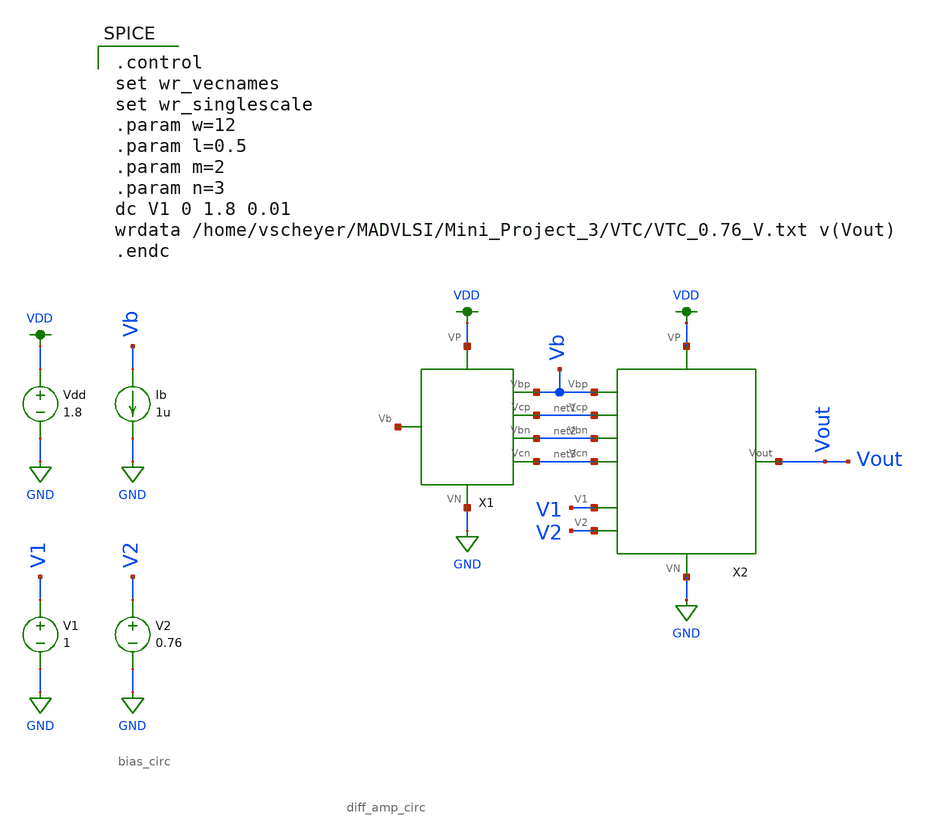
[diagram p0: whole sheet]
** sch_path: Mini_Project_3/diff_amp_VTC.sch
**.subckt diff_amp_VTC
Vdd VDD GND 1.8
Ib Vb GND 1u
V1 V1 GND 1
V2 V2 GND 0.76
X1 VDD GND net3 net2 net1 Vb net4 bias_circ
X2 Vb net1 net2 net3 Vout GND VDD V1 V2 diff_amp_circ
**** begin user architecture code

.option wnflag=1
.lib ~/skywater/skywater-pdk/libraries/sky130_fd_pr_ngspice/latest/models/sky130.lib.spice tt


.control
set wr_vecnames
set wr_singlescale
.param w=12
.param l=0.5
.param m=2
.param n=3
dc V1 0 1.8 0.01
wrdata /home/vscheyer/MADVLSI/Mini_Project_3/VTC/VTC_0.76_V.txt v(Vout)
.endc

**** end user architecture code
**.ends
.GLOBAL VDD
.GLOBAL GND
.end
